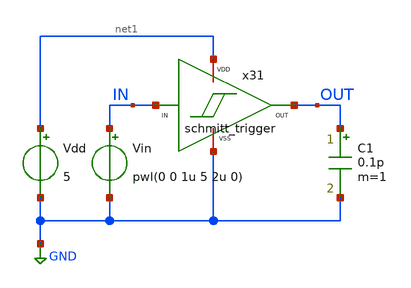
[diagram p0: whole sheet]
** sch_path: member_project/imager/YuMaehashi/design/tb_schmitt_trigger.sch
**.subckt tb_schmitt_trigger
Vin IN GND pwl(0 0 1u 5 2u 0)
Vdd net1 GND 5
x31 IN OUT net1 GND schmitt_trigger
C1 OUT GND 0.1p m=1
**** begin user architecture code
 .include $::LIB/ip62_models


.option savecurrents
.temp 40

.control
set units=degree
save all

alterparam vthMN = 0 ; Slow:0.1, Fast:-0.1
alterparam vthMP = 0 ; Slow:-0.1, Fast:0.1
reset

tran 1n 2u
plot v(IN) v(OUT)
.endc

**** end user architecture code
**.ends

* expanding   symbol:  2026_imager/schmitt_trigger.sym # of pins=4
** sym_path: member_project/imager/YuMaehashi/design/schmitt_trigger.sym
** sch_path: member_project/imager/YuMaehashi/design/schmitt_trigger.sch
.subckt schmitt_trigger IN OUT VDD VSS
*.opin OUT
*.ipin IN
*.iopin VDD
*.iopin VSS
XXMN1 net1 IN VSS VSS NMOS w=3.4u l=1u nrd=0 nrs=0 m=1
XXMN2 OUT IN net1 VSS NMOS w=3.4u l=1u nrd=0 nrs=0 m=1
XXMP2 OUT IN net2 VDD PMOS w=10.2u l=1u nrd=0 nrs=0 m=1
XXMP1 net2 IN VDD VDD PMOS w=10.2u l=1u nrd=0 nrs=0 m=1
XXMP3 VSS OUT net2 VDD PMOS w=10.2u l=1u nrd=0 nrs=0 m=1
XXMN3 VDD OUT net1 VSS NMOS w=3.4u l=1u nrd=0 nrs=0 m=1
.ends

.GLOBAL GND
.end
